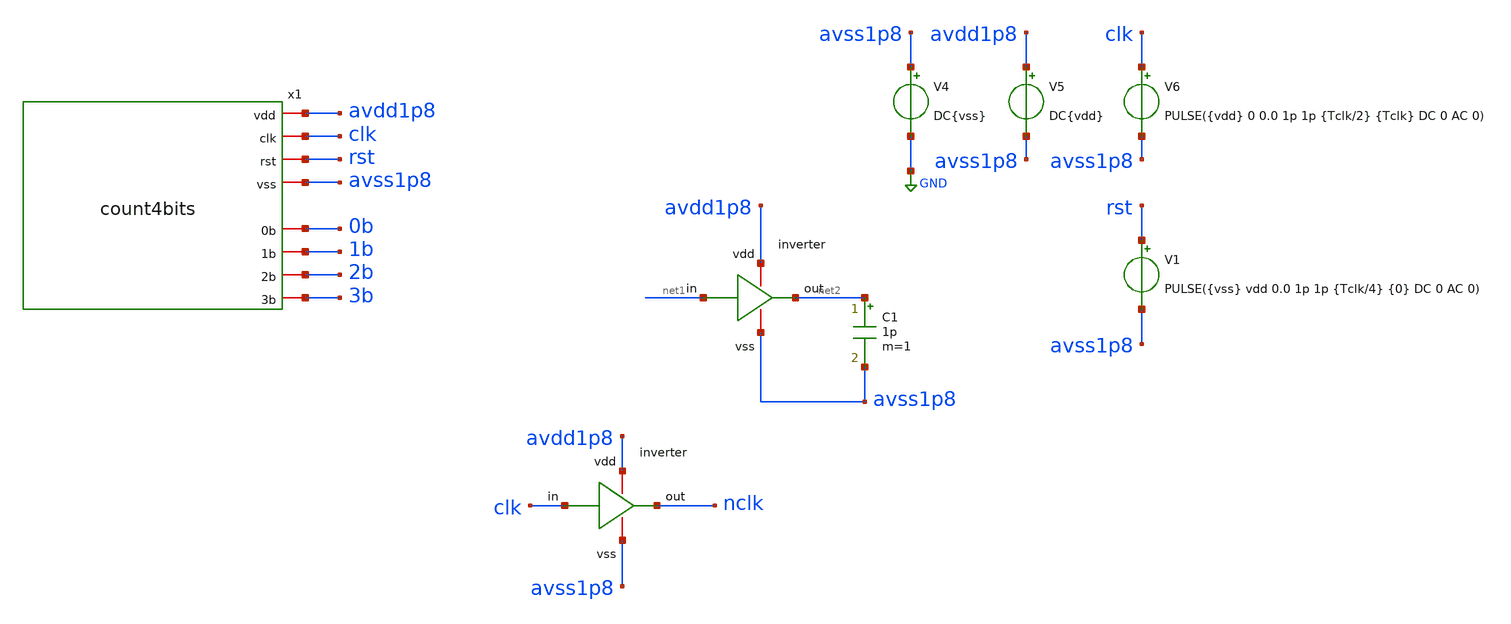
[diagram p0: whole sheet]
** sch_path: verification/testbenches/tb_count4bits.sch
**.subckt tb_count4bits
C1 net2 avss1p8 1p m=1
V4 avss1p8 GND DC{vss}
V5 avdd1p8 avss1p8 DC{vdd}
V6 clk avss1p8 PULSE({vdd} 0 0.0 1p 1p {Tclk/2} {Tclk} DC 0 AC 0)
x2 avdd1p8 net2 net1 avss1p8 inverter
x3 avdd1p8 nclk clk avss1p8 inverter
x1 avdd1p8 clk rst avss1p8 0b 1b 2b 3b count4bits
V1 rst avss1p8 PULSE({vss} vdd 0.0 1p 1p {Tclk/4} {0} DC 0 AC 0)
**** begin user architecture code


* Circuit Parameters
.param vdd = 1.2
.param vss = 0.0
.param Tclk = 10n
.options TEMP = 27.0
* Include Models - IHP SG13G2
.lib cornerMOSlv.lib mos_tt
* OP Parameters & Singals to save
.save all
*Simulations
.control
tran 0.01u 100n
setplot tran1
plot v(clk) v(0b)+1.2 v(1b)+2.4 v(2b)+3.6 v(3b)+4.8 v(rst) + 6
reset
dc V6 0 1.2 0.01
setplot dc
set filetype = ascii
write dcsweep.raw
.endc
.end


**** end user architecture code
**.ends
.GLOBAL GND
.end
